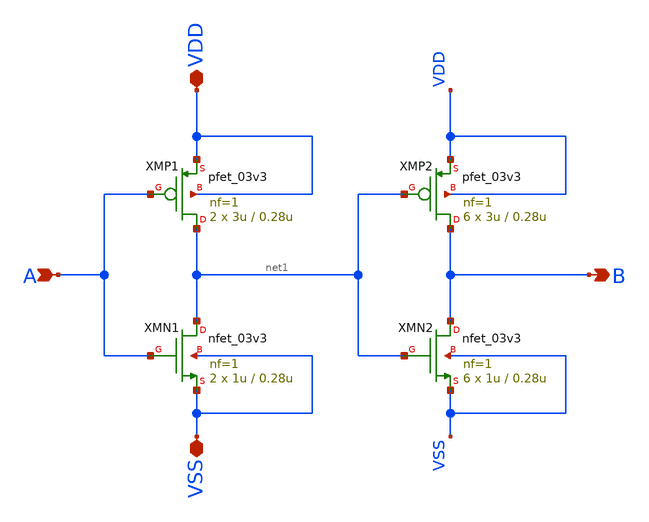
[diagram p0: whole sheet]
** sch_path: designs/DS_modulator/gate_buf_L0d28/xschem/gate_buf_L0d28.sch
**.subckt gate_buf_L0d28 B A VDD VSS
*.opin B
*.ipin A
*.iopin VDD
*.iopin VSS
XMN1 net1 A VSS VSS nfet_03v3 L=0.28u W=1u nf=1 ad='int((nf+1)/2) * W/nf * 0.18u' as='int((nf+2)/2) * W/nf * 0.18u'
+ pd='2*int((nf+1)/2) * (W/nf + 0.18u)' ps='2*int((nf+2)/2) * (W/nf + 0.18u)' nrd='0.18u / W' nrs='0.18u / W'
+ sa=0 sb=0 sd=0 m=2
XMP1 net1 A VDD VDD pfet_03v3 L=0.28u W=3u nf=1 ad='int((nf+1)/2) * W/nf * 0.18u' as='int((nf+2)/2) * W/nf * 0.18u'
+ pd='2*int((nf+1)/2) * (W/nf + 0.18u)' ps='2*int((nf+2)/2) * (W/nf + 0.18u)' nrd='0.18u / W' nrs='0.18u / W'
+ sa=0 sb=0 sd=0 m=2
XMN2 B net1 VSS VSS nfet_03v3 L=0.28u W=1u nf=1 ad='int((nf+1)/2) * W/nf * 0.18u' as='int((nf+2)/2) * W/nf * 0.18u'
+ pd='2*int((nf+1)/2) * (W/nf + 0.18u)' ps='2*int((nf+2)/2) * (W/nf + 0.18u)' nrd='0.18u / W' nrs='0.18u / W'
+ sa=0 sb=0 sd=0 m=6
XMP2 B net1 VDD VDD pfet_03v3 L=0.28u W=3u nf=1 ad='int((nf+1)/2) * W/nf * 0.18u' as='int((nf+2)/2) * W/nf * 0.18u'
+ pd='2*int((nf+1)/2) * (W/nf + 0.18u)' ps='2*int((nf+2)/2) * (W/nf + 0.18u)' nrd='0.18u / W' nrs='0.18u / W'
+ sa=0 sb=0 sd=0 m=6
**.ends
.end
